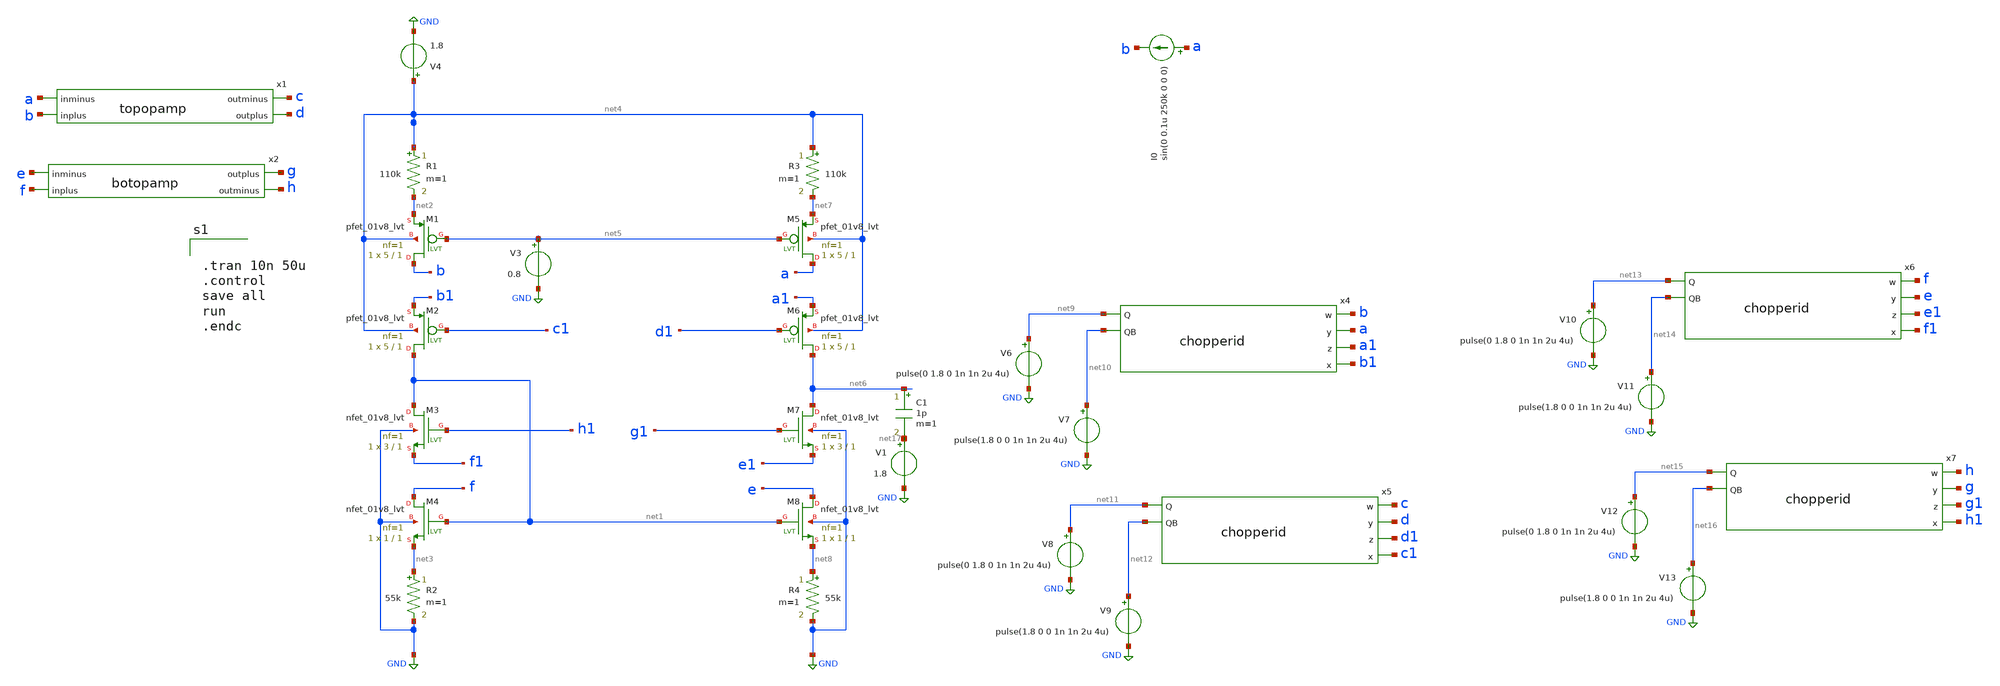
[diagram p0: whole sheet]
** sch_path: currentb.sch
**.subckt currentb
XM1 b net5 net2 net4 sky130_fd_pr__pfet_01v8_lvt L=1 W=5 nf=1 ad='int((nf+1)/2) * W/nf * 0.29' as='int((nf+2)/2) * W/nf * 0.29'
+ pd='2*int((nf+1)/2) * (W/nf + 0.29)' ps='2*int((nf+2)/2) * (W/nf + 0.29)' nrd='0.29 / W' nrs='0.29 / W'
+ sa=0 sb=0 sd=0 mult=1 m=1
XM2 net1 c1 b1 net4 sky130_fd_pr__pfet_01v8_lvt L=1 W=5 nf=1 ad='int((nf+1)/2) * W/nf * 0.29' as='int((nf+2)/2) * W/nf * 0.29'
+ pd='2*int((nf+1)/2) * (W/nf + 0.29)' ps='2*int((nf+2)/2) * (W/nf + 0.29)' nrd='0.29 / W' nrs='0.29 / W'
+ sa=0 sb=0 sd=0 mult=1 m=1
XM3 net1 h1 f1 GND sky130_fd_pr__nfet_01v8_lvt L=1 W=3 nf=1 ad='int((nf+1)/2) * W/nf * 0.29' as='int((nf+2)/2) * W/nf * 0.29'
+ pd='2*int((nf+1)/2) * (W/nf + 0.29)' ps='2*int((nf+2)/2) * (W/nf + 0.29)' nrd='0.29 / W' nrs='0.29 / W'
+ sa=0 sb=0 sd=0 mult=1 m=1
XM4 f net1 net3 GND sky130_fd_pr__nfet_01v8_lvt L=1 W=1 nf=1 ad='int((nf+1)/2) * W/nf * 0.29' as='int((nf+2)/2) * W/nf * 0.29'
+ pd='2*int((nf+1)/2) * (W/nf + 0.29)' ps='2*int((nf+2)/2) * (W/nf + 0.29)' nrd='0.29 / W' nrs='0.29 / W'
+ sa=0 sb=0 sd=0 mult=1 m=1
R1 net4 net2 110k m=1
R2 net3 GND 55k m=1
V3 net5 GND 0.8
V4 net4 GND 1.8
XM5 a net5 net7 net4 sky130_fd_pr__pfet_01v8_lvt L=1 W=5 nf=1 ad='int((nf+1)/2) * W/nf * 0.29' as='int((nf+2)/2) * W/nf * 0.29'
+ pd='2*int((nf+1)/2) * (W/nf + 0.29)' ps='2*int((nf+2)/2) * (W/nf + 0.29)' nrd='0.29 / W' nrs='0.29 / W'
+ sa=0 sb=0 sd=0 mult=1 m=1
XM6 net6 d1 a1 net4 sky130_fd_pr__pfet_01v8_lvt L=1 W=5 nf=1 ad='int((nf+1)/2) * W/nf * 0.29' as='int((nf+2)/2) * W/nf * 0.29'
+ pd='2*int((nf+1)/2) * (W/nf + 0.29)' ps='2*int((nf+2)/2) * (W/nf + 0.29)' nrd='0.29 / W' nrs='0.29 / W'
+ sa=0 sb=0 sd=0 mult=1 m=1
XM7 net6 g1 e1 GND sky130_fd_pr__nfet_01v8_lvt L=1 W=3 nf=1 ad='int((nf+1)/2) * W/nf * 0.29' as='int((nf+2)/2) * W/nf * 0.29'
+ pd='2*int((nf+1)/2) * (W/nf + 0.29)' ps='2*int((nf+2)/2) * (W/nf + 0.29)' nrd='0.29 / W' nrs='0.29 / W'
+ sa=0 sb=0 sd=0 mult=1 m=1
XM8 e net1 net8 GND sky130_fd_pr__nfet_01v8_lvt L=1 W=1 nf=1 ad='int((nf+1)/2) * W/nf * 0.29' as='int((nf+2)/2) * W/nf * 0.29'
+ pd='2*int((nf+1)/2) * (W/nf + 0.29)' ps='2*int((nf+2)/2) * (W/nf + 0.29)' nrd='0.29 / W' nrs='0.29 / W'
+ sa=0 sb=0 sd=0 mult=1 m=1
R3 net4 net7 110k m=1
R4 net8 GND 55k m=1
x1 a b c d topopamp
x2 g h e f botopamp
x4 net9 b a net10 a1 b1 chopperid
V6 net9 GND pulse(0 1.8 0 1n 1n 2u 4u)
V7 net10 GND pulse(1.8 0 0 1n 1n 2u 4u)
x5 net11 c d net12 d1 c1 chopperid
V8 net11 GND pulse(0 1.8 0 1n 1n 2u 4u)
V9 net12 GND pulse(1.8 0 0 1n 1n 2u 4u)
x6 net13 f e net14 e1 f1 chopperid
V10 net13 GND pulse(0 1.8 0 1n 1n 2u 4u)
V11 net14 GND pulse(1.8 0 0 1n 1n 2u 4u)
x7 net15 h g net16 g1 h1 chopperid
V12 net15 GND pulse(0 1.8 0 1n 1n 2u 4u)
V13 net16 GND pulse(1.8 0 0 1n 1n 2u 4u)
I0 a b sin(0 0.1u 250k 0 0 0)
C1 net6 net17 1p m=1
V1 net17 GND 1.8
**** begin user architecture code

*.lib ~/open_pdks/sky130/sky130A/libs.tech/ngspice/sky130.lib.spice tt
*.lib ~/open_pdks/sky130/sky130A/libs.tech/ngspice/sky130.lib.spice tt
.param mc_mm_switch=0
.param mc_pr_switch=0

.include ~/open_pdks/sky130/sky130A/libs.tech/ngspice/corners/tt/nonfet.spice


*model
.include ~/open_pdks/sky130/sky130A/libs.tech/ngspice/all.spice

*mosfet
.include ~/open_pdks/sky130/sky130A/libs.ref/sky130_fd_pr/spice/sky130_fd_pr__pfet_01v8_lvt__tt.corner.spice
.inclued ~/open_pdks/sky130/sky130A/libs.ref/sky130_fd_pr/spice/sky130_fd_pr__nfet_01v8_lvt__tt.corner.spice

*mismatch parameters
.include ~/open_pdks/sky130/sky130A/libs.ref/sky130_fd_pr/spice/sky130_fd_pr__pfet_01v8_lvt__mismatch.corner.spice
.include ~/open_pdks/sky130/sky130A/libs.ref/sky130_fd_pr/spice/sky130_fd_pr__nfet_01v8_lvt__mismatch.corner.spice



.MODEL swmod SW(VT=0.9 VH=0 RON=1 ROFF=10000000000)


.tran 10n 50u
.control
save all
run
.endc

**** end user architecture code
**.ends

* expanding   symbol:  /home/cegrahul/Desktop/SSCS/topopamp.sym # of pins=4
** sym_path: topopamp.sym
** sch_path: topopamp.sch
.subckt topopamp inminus inplus outminus outplus
*.ipin inplus
*.ipin inminus
*.opin outplus
*.opin outminus
XM1 outminus net1 GND GND sky130_fd_pr__nfet_01v8_lvt L=1 W=1 nf=1 ad='int((nf+1)/2) * W/nf * 0.29' as='int((nf+2)/2) * W/nf * 0.29'
+ pd='2*int((nf+1)/2) * (W/nf + 0.29)' ps='2*int((nf+2)/2) * (W/nf + 0.29)' nrd='0.29 / W' nrs='0.29 / W'
+ sa=0 sb=0 sd=0 mult=1 m=1
XM2 outplus net1 GND GND sky130_fd_pr__nfet_01v8_lvt L=1 W=1 nf=1 ad='int((nf+1)/2) * W/nf * 0.29' as='int((nf+2)/2) * W/nf * 0.29'
+ pd='2*int((nf+1)/2) * (W/nf + 0.29)' ps='2*int((nf+2)/2) * (W/nf + 0.29)' nrd='0.29 / W' nrs='0.29 / W'
+ sa=0 sb=0 sd=0 mult=1 m=1
XM3 outminus inplus net2 net3 sky130_fd_pr__pfet_01v8_lvt L=1 W=1 nf=1 ad='int((nf+1)/2) * W/nf * 0.29'
+ as='int((nf+2)/2) * W/nf * 0.29' pd='2*int((nf+1)/2) * (W/nf + 0.29)' ps='2*int((nf+2)/2) * (W/nf + 0.29)'
+ nrd='0.29 / W' nrs='0.29 / W' sa=0 sb=0 sd=0 mult=2 m=2
XM4 outplus inminus net2 net3 sky130_fd_pr__pfet_01v8_lvt L=1 W=1 nf=1 ad='int((nf+1)/2) * W/nf * 0.29'
+ as='int((nf+2)/2) * W/nf * 0.29' pd='2*int((nf+1)/2) * (W/nf + 0.29)' ps='2*int((nf+2)/2) * (W/nf + 0.29)'
+ nrd='0.29 / W' nrs='0.29 / W' sa=0 sb=0 sd=0 mult=2 m=2
R1 net3 net2 165k m=1
V1 net3 GND 1.8
V2 net1 GND 0.5236
.ends


* expanding   symbol:  /home/cegrahul/Desktop/SSCS/botopamp.sym # of pins=4
** sym_path: botopamp.sym
** sch_path: botopamp.sch
.subckt botopamp outplus outminus inminus inplus
*.ipin inplus
*.opin outminus
*.opin outplus
*.ipin inminus
XM1 outminus net5 net1 net3 sky130_fd_pr__pfet_01v8_lvt L=1 W=0.55 nf=1 ad='int((nf+1)/2) * W/nf * 0.29'
+ as='int((nf+2)/2) * W/nf * 0.29' pd='2*int((nf+1)/2) * (W/nf + 0.29)' ps='2*int((nf+2)/2) * (W/nf + 0.29)'
+ nrd='0.29 / W' nrs='0.29 / W' sa=0 sb=0 sd=0 mult=1 m=1
XM2 outplus net5 net2 net3 sky130_fd_pr__pfet_01v8_lvt L=1 W=0.55 nf=1 ad='int((nf+1)/2) * W/nf * 0.29'
+ as='int((nf+2)/2) * W/nf * 0.29' pd='2*int((nf+1)/2) * (W/nf + 0.29)' ps='2*int((nf+2)/2) * (W/nf + 0.29)'
+ nrd='0.29 / W' nrs='0.29 / W' sa=0 sb=0 sd=0 mult=1 m=1
XM3 outminus inplus net4 GND sky130_fd_pr__nfet_01v8_lvt L=2 W=1 nf=1 ad='int((nf+1)/2) * W/nf * 0.29'
+ as='int((nf+2)/2) * W/nf * 0.29' pd='2*int((nf+1)/2) * (W/nf + 0.29)' ps='2*int((nf+2)/2) * (W/nf + 0.29)'
+ nrd='0.29 / W' nrs='0.29 / W' sa=0 sb=0 sd=0 mult=1 m=1
XM4 outplus inminus net4 GND sky130_fd_pr__nfet_01v8_lvt L=2 W=1 nf=1 ad='int((nf+1)/2) * W/nf * 0.29'
+ as='int((nf+2)/2) * W/nf * 0.29' pd='2*int((nf+1)/2) * (W/nf + 0.29)' ps='2*int((nf+2)/2) * (W/nf + 0.29)'
+ nrd='0.29 / W' nrs='0.29 / W' sa=0 sb=0 sd=0 mult=1 m=1
R1 net3 net1 330k m=1
R2 net3 net2 330k m=1
R3 net4 GND 165k m=1
V1 net5 GND 0.995
V3 net3 GND 1.8
.ends


* expanding   symbol:  /home/cegrahul/Desktop/SSCS/chopperid.sym # of pins=6
** sym_path: chopperid.sym
** sch_path: chopperid.sch
.subckt chopperid Q w y QB z x
*.ipin Q
*.ipin QB
*.opin w
*.opin y
*.opin x
*.opin z
S1 w x Q GND swmod
S2 w z QB GND swmod
S3 y x QB GND swmod
S4 y z Q GND swmod
.ends

.GLOBAL GND
.end
